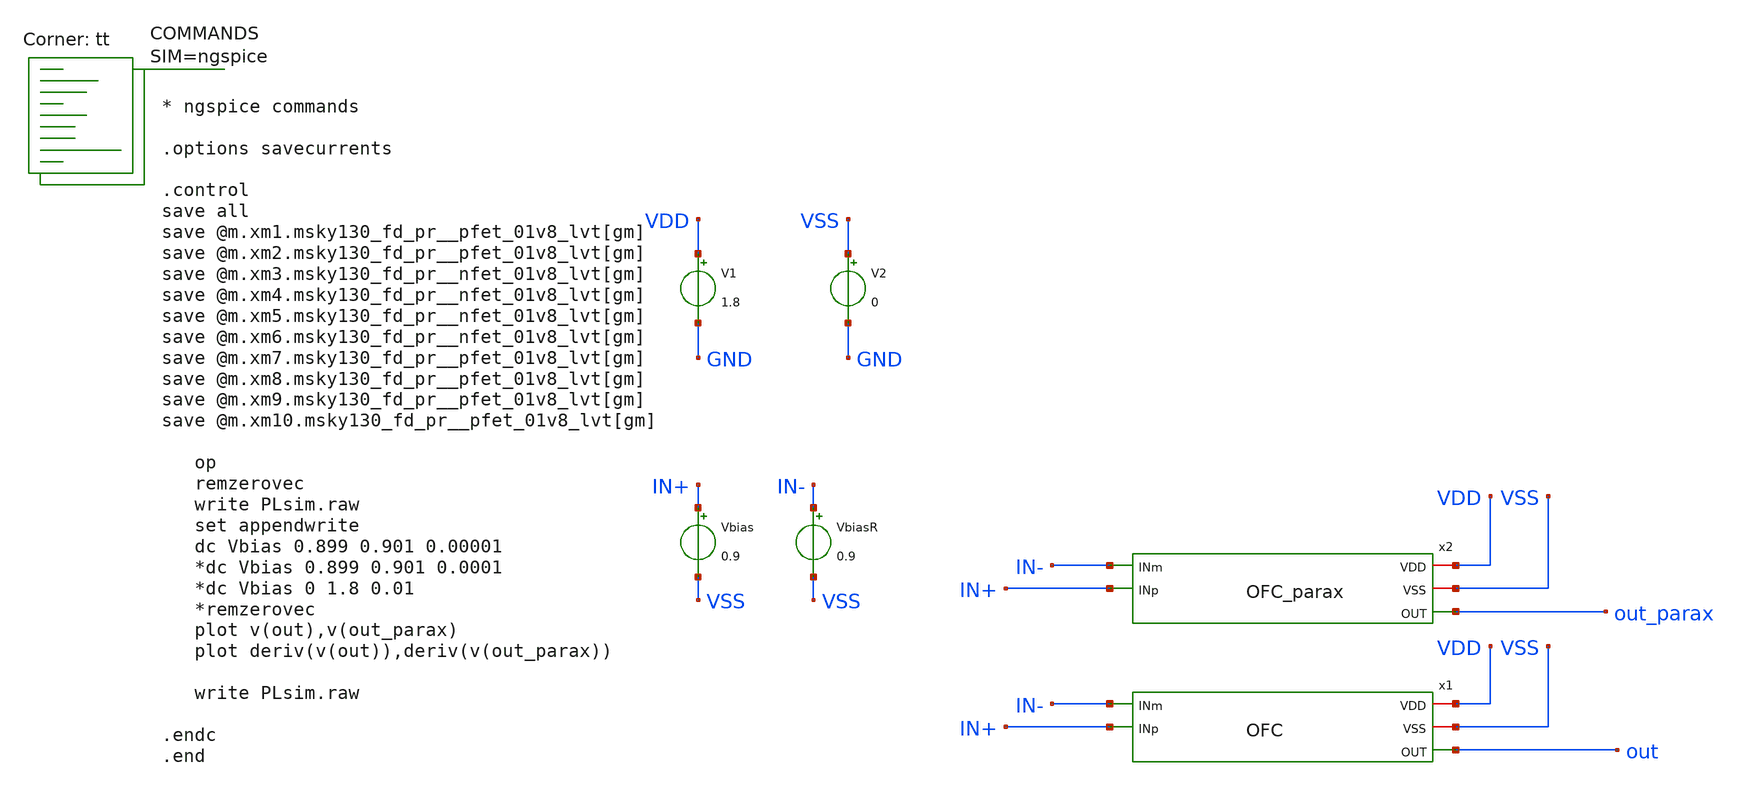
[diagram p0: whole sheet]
** sch_path: tt_um_NE567Mixer28/xschem/PLsim.sch
**.subckt PLsim
x1 VDD VSS out IN- IN+ OFC
x2 VDD VSS out_parax IN- IN+ OFC_parax
V1 VDD GND 1.8
Vbias IN+ VSS 0.9
VbiasR IN- VSS 0.9
V2 VSS GND 0
**** begin user architecture code



* ngspice commands

.options savecurrents

.control
save all
save @m.xm1.msky130_fd_pr__pfet_01v8_lvt[gm]
save @m.xm2.msky130_fd_pr__pfet_01v8_lvt[gm]
save @m.xm3.msky130_fd_pr__nfet_01v8_lvt[gm]
save @m.xm4.msky130_fd_pr__nfet_01v8_lvt[gm]
save @m.xm5.msky130_fd_pr__nfet_01v8_lvt[gm]
save @m.xm6.msky130_fd_pr__nfet_01v8_lvt[gm]
save @m.xm7.msky130_fd_pr__pfet_01v8_lvt[gm]
save @m.xm8.msky130_fd_pr__pfet_01v8_lvt[gm]
save @m.xm9.msky130_fd_pr__pfet_01v8_lvt[gm]
save @m.xm10.msky130_fd_pr__pfet_01v8_lvt[gm]

   op
   remzerovec
   write PLsim.raw
   set appendwrite
   dc Vbias 0.899 0.901 0.00001
   *dc Vbias 0.899 0.901 0.0001
   *dc Vbias 0 1.8 0.01
   *remzerovec
   plot v(out),v(out_parax)
   plot deriv(v(out)),deriv(v(out_parax))

   write PLsim.raw

.endc
.end



.lib $::SKYWATER_MODELS/sky130.lib.spice tt
**** end user architecture code
**.ends

* expanding   symbol:  OFC.sym # of pins=5
** sym_path: tt_um_NE567Mixer28/xschem/OFC.sym
** sch_path: tt_um_NE567Mixer28/xschem/OFC.sch
.subckt OFC VDD VSS OUT INm INp
*.iopin VDD
*.iopin VSS
*.ipin INp
*.ipin INm
*.opin OUT
XM11 S Vb VDD VDD sky130_fd_pr__pfet_01v8_lvt L=1 W=60 nf=6 ad='int((nf+1)/2) * W/nf * 0.29' as='int((nf+2)/2) * W/nf * 0.29'
+ pd='2*int((nf+1)/2) * (W/nf + 0.29)' ps='2*int((nf+2)/2) * (W/nf + 0.29)' nrd='0.29 / W' nrs='0.29 / W'
+ sa=0 sb=0 sd=0 mult=2 m=2
XM1 D1 INp S S sky130_fd_pr__pfet_01v8_lvt L=10 W=25 nf=2 ad='int((nf+1)/2) * W/nf * 0.29' as='int((nf+2)/2) * W/nf * 0.29'
+ pd='2*int((nf+1)/2) * (W/nf + 0.29)' ps='2*int((nf+2)/2) * (W/nf + 0.29)' nrd='0.29 / W' nrs='0.29 / W'
+ sa=0 sb=0 sd=0 mult=2 m=2
XM2 D2 INm S S sky130_fd_pr__pfet_01v8_lvt L=10 W=25 nf=2 ad='int((nf+1)/2) * W/nf * 0.29' as='int((nf+2)/2) * W/nf * 0.29'
+ pd='2*int((nf+1)/2) * (W/nf + 0.29)' ps='2*int((nf+2)/2) * (W/nf + 0.29)' nrd='0.29 / W' nrs='0.29 / W'
+ sa=0 sb=0 sd=0 mult=2 m=2
XM3 OUT Vc1 D2 VSS sky130_fd_pr__nfet_01v8_lvt L=1 W=4 nf=1 ad='int((nf+1)/2) * W/nf * 0.29' as='int((nf+2)/2) * W/nf * 0.29'
+ pd='2*int((nf+1)/2) * (W/nf + 0.29)' ps='2*int((nf+2)/2) * (W/nf + 0.29)' nrd='0.29 / W' nrs='0.29 / W'
+ sa=0 sb=0 sd=0 mult=1 m=1
XM4 D2 Vc VSS VSS sky130_fd_pr__nfet_01v8_lvt L=1 W=2.8 nf=1 ad='int((nf+1)/2) * W/nf * 0.29' as='int((nf+2)/2) * W/nf * 0.29'
+ pd='2*int((nf+1)/2) * (W/nf + 0.29)' ps='2*int((nf+2)/2) * (W/nf + 0.29)' nrd='0.29 / W' nrs='0.29 / W'
+ sa=0 sb=0 sd=0 mult=1 m=1
XM5 D1 Vc VSS VSS sky130_fd_pr__nfet_01v8_lvt L=1 W=2.8 nf=1 ad='int((nf+1)/2) * W/nf * 0.29' as='int((nf+2)/2) * W/nf * 0.29'
+ pd='2*int((nf+1)/2) * (W/nf + 0.29)' ps='2*int((nf+2)/2) * (W/nf + 0.29)' nrd='0.29 / W' nrs='0.29 / W'
+ sa=0 sb=0 sd=0 mult=1 m=1
XM6 G Vc1 D1 VSS sky130_fd_pr__nfet_01v8_lvt L=1 W=4 nf=1 ad='int((nf+1)/2) * W/nf * 0.29' as='int((nf+2)/2) * W/nf * 0.29'
+ pd='2*int((nf+1)/2) * (W/nf + 0.29)' ps='2*int((nf+2)/2) * (W/nf + 0.29)' nrd='0.29 / W' nrs='0.29 / W'
+ sa=0 sb=0 sd=0 mult=1 m=1
XM7 G Vc2 D9 D9 sky130_fd_pr__pfet_01v8_lvt L=2.23 W=3 nf=1 ad='int((nf+1)/2) * W/nf * 0.29' as='int((nf+2)/2) * W/nf * 0.29'
+ pd='2*int((nf+1)/2) * (W/nf + 0.29)' ps='2*int((nf+2)/2) * (W/nf + 0.29)' nrd='0.29 / W' nrs='0.29 / W'
+ sa=0 sb=0 sd=0 mult=1 m=1
XM9 D9 G VDD VDD sky130_fd_pr__pfet_01v8_lvt L=2.23 W=4 nf=1 ad='int((nf+1)/2) * W/nf * 0.29' as='int((nf+2)/2) * W/nf * 0.29'
+ pd='2*int((nf+1)/2) * (W/nf + 0.29)' ps='2*int((nf+2)/2) * (W/nf + 0.29)' nrd='0.29 / W' nrs='0.29 / W'
+ sa=0 sb=0 sd=0 mult=1 m=1
XM8 D10 G VDD VDD sky130_fd_pr__pfet_01v8_lvt L=2.23 W=4 nf=1 ad='int((nf+1)/2) * W/nf * 0.29' as='int((nf+2)/2) * W/nf * 0.29'
+ pd='2*int((nf+1)/2) * (W/nf + 0.29)' ps='2*int((nf+2)/2) * (W/nf + 0.29)' nrd='0.29 / W' nrs='0.29 / W'
+ sa=0 sb=0 sd=0 mult=1 m=1
XM10 OUT Vc2 D10 D10 sky130_fd_pr__pfet_01v8_lvt L=2.23 W=3 nf=1 ad='int((nf+1)/2) * W/nf * 0.29' as='int((nf+2)/2) * W/nf * 0.29'
+ pd='2*int((nf+1)/2) * (W/nf + 0.29)' ps='2*int((nf+2)/2) * (W/nf + 0.29)' nrd='0.29 / W' nrs='0.29 / W'
+ sa=0 sb=0 sd=0 mult=1 m=1
XR2 Vb VDD VSS sky130_fd_pr__res_xhigh_po_0p35 L=5 mult=1 m=1
XR3 VSS Vb VSS sky130_fd_pr__res_xhigh_po_0p35 L=13.2 mult=1 m=1
XR1 Vc VDD VSS sky130_fd_pr__res_xhigh_po_0p35 L=5 mult=1 m=1
XR4 VSS Vc VSS sky130_fd_pr__res_xhigh_po_0p35 L=3.07 mult=1 m=1
XR5 Vc1 VDD VSS sky130_fd_pr__res_xhigh_po_0p35 L=5 mult=1 m=1
XR6 VSS Vc1 VSS sky130_fd_pr__res_xhigh_po_0p35 L=13.2 mult=1 m=1
XR7 Vc2 VDD VSS sky130_fd_pr__res_xhigh_po_0p35 L=5 mult=1 m=1
XR8 VSS Vc2 VSS sky130_fd_pr__res_xhigh_po_0p35 L=1.6 mult=1 m=1
.ends


* expanding   symbol:  OFC_parax.sym # of pins=5
** sym_path: tt_um_NE567Mixer28/xschem/OFC.sym
.include [file normalize ../mag/OFC.sim.spice]
.end
